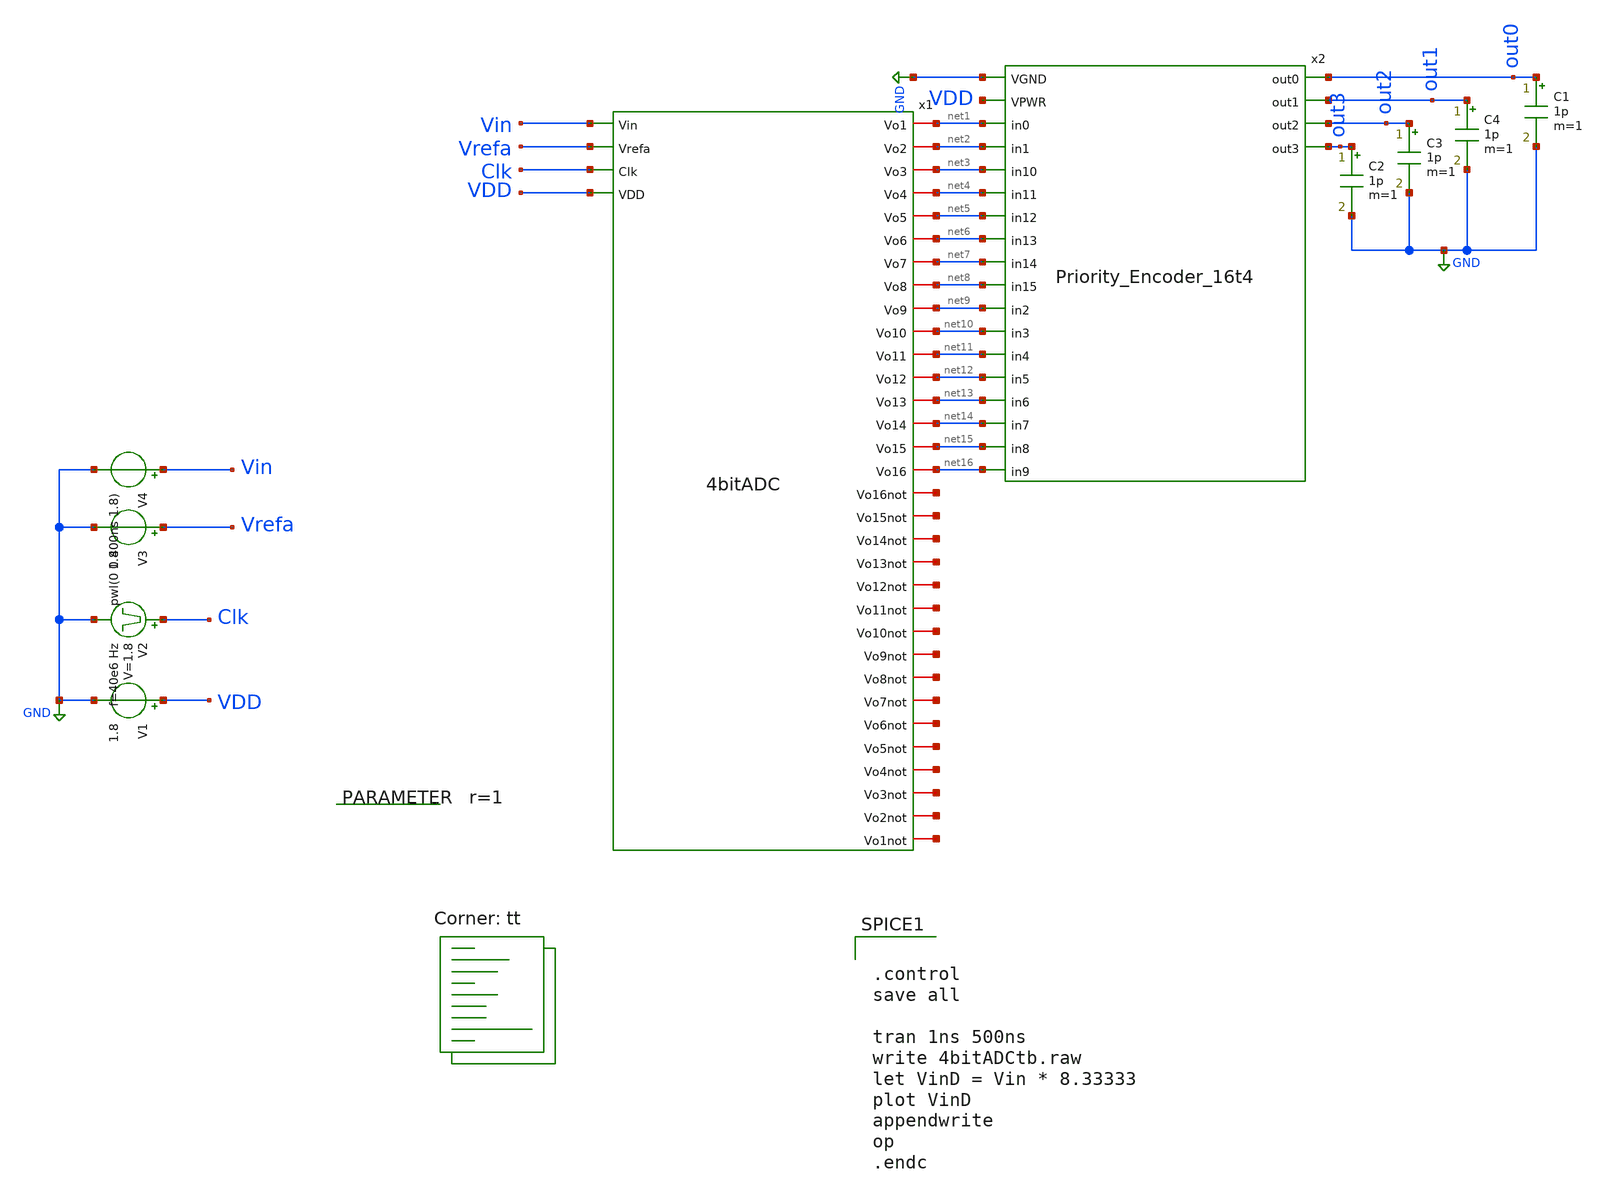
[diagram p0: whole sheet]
** sch_path: xschem/to_send/4bitADCtb.sch
**.subckt 4bitADCtb
V1 VDD GND 1.8
V3 Vrefa GND 1.8
.save i(v3)
V4 Vin GND pwl(0 0 400ns 1.8)
.param r=1
V2 Clk GND pulse 0 1.8 '0.495/ 40e6 ' '0.01/40e6 ' '0.01/40e6 ' '0.49/40e6 ' '1/40e6 '
x2 GND VDD net1 net2 net3 net4 net5 net6 net7 net8 net9 net10 net11 net12 net13 net14 net15 net16
+ out0 out1 out2 out3 Priority_Encoder_16t4
x1 net1 net2 Vin net3 Vrefa net4 net5 Clk net6 net7 VDD net8 net9 net10 net11 net12 net13 net14
+ net15 net16 net17 net18 net19 net20 net21 net22 net23 net24 net25 net26 net27 net28 net29 net30 net31
+ net32 4bitADC
C1 out0 GND 1p m=1
C2 out3 GND 1p m=1
C3 out2 GND 1p m=1
C4 out1 GND 1p m=1
**** begin user architecture code
.lib $::SKYWATER_MODELS/sky130.lib.spice tt


.control
save all

tran 1ns 500ns
write 4bitADCtb.raw
let VinD = Vin * 8.33333
plot VinD
appendwrite
op
.endc



** opencircuitdesign pdks install
.include $::SKYWATER_STDCELLS/sky130_fd_sc_hd.spice


**** end user architecture code
**.ends
.GLOBAL GND
.end
